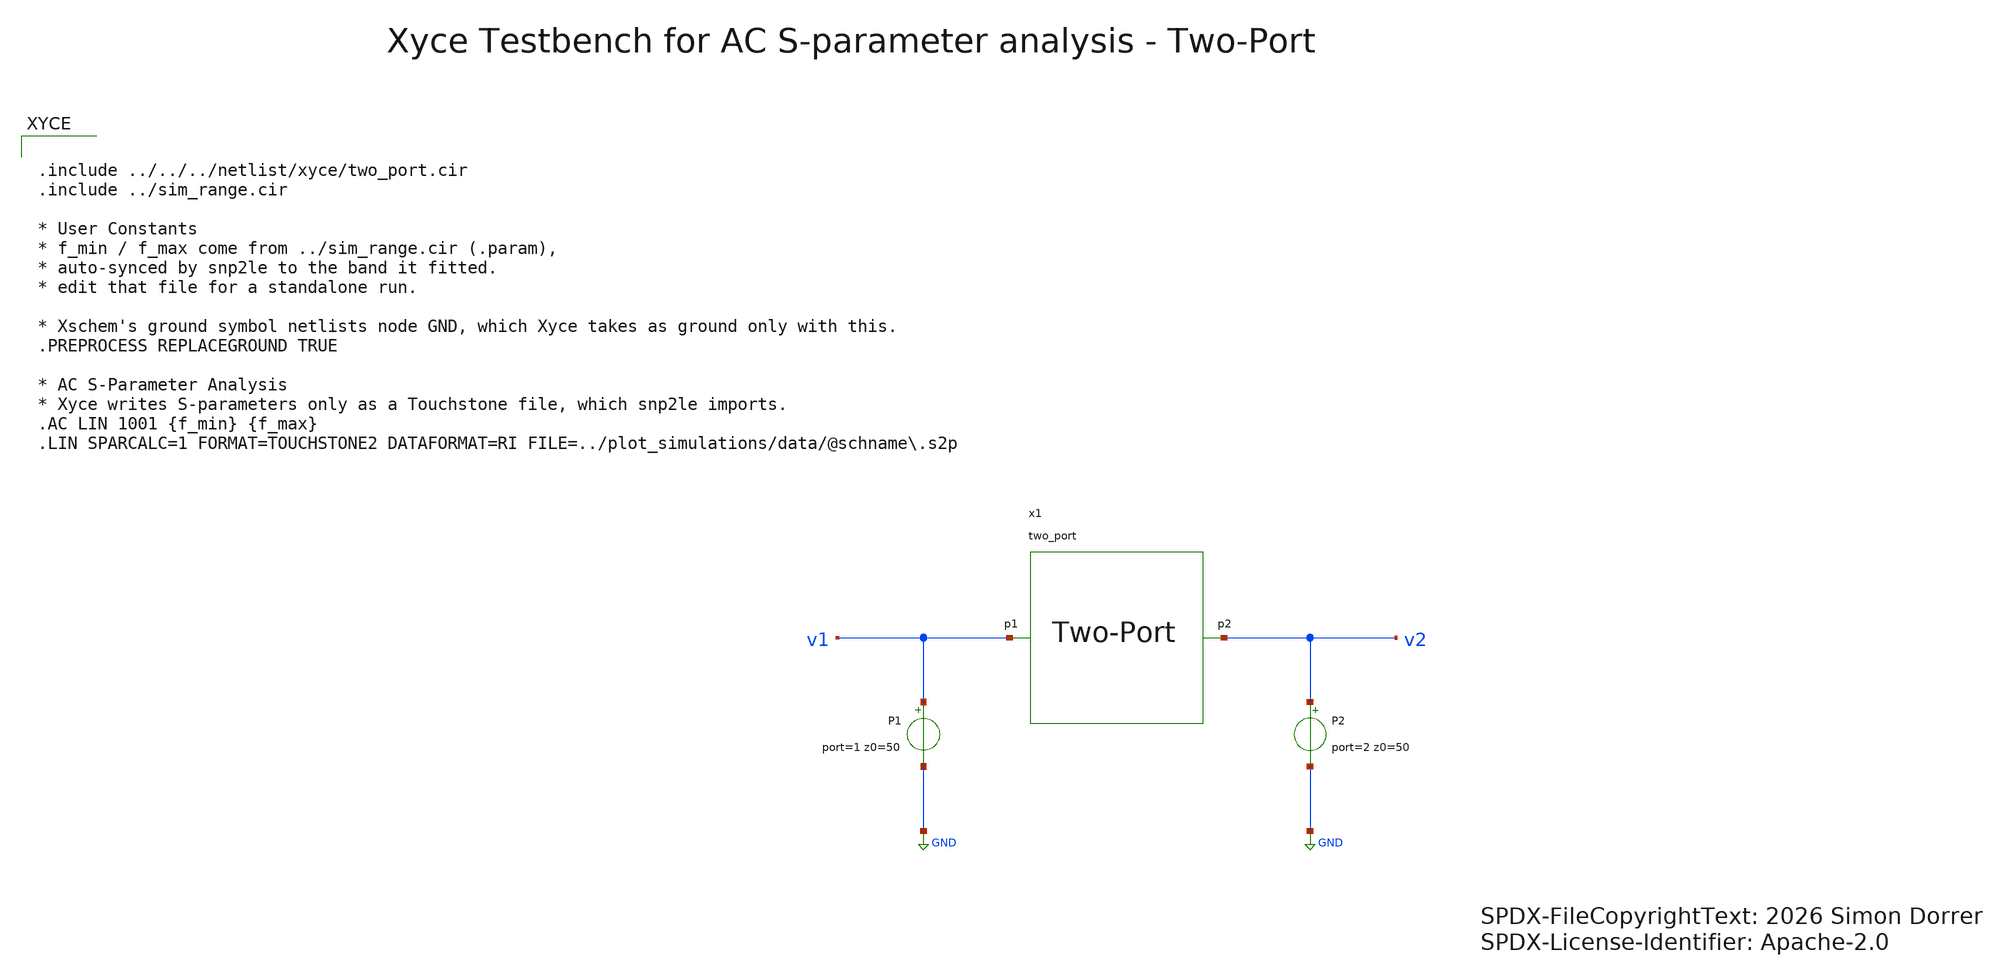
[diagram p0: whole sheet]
** sch_path: testbenches/xschem/two_port_tb_acsp_xyce.sch
* SPDX-FileCopyrightText: 2026 Simon Dorrer
* SPDX-License-Identifier: Apache-2.0
**.subckt two_port_tb_acsp_xyce
P1 v1 GND port=1 z0=50
P2 v2 GND port=2 z0=50
x1 v1 v2 two_port
**** begin user architecture code


.include ../../../netlist/xyce/two_port.cir
.include ../sim_range.cir

* User Constants
* f_min / f_max come from ../sim_range.cir (.param),
* auto-synced by snp2le to the band it fitted.
* edit that file for a standalone run.

* Xschem's ground symbol netlists node GND, which Xyce takes as ground only with this.
.PREPROCESS REPLACEGROUND TRUE

* AC S-Parameter Analysis
* Xyce writes S-parameters only as a Touchstone file, which snp2le imports.
.AC LIN 1001 {f_min} {f_max}
.LIN SPARCALC=1 FORMAT=TOUCHSTONE2 DATAFORMAT=RI FILE=../plot_simulations/data/@schname\.s2p


**** end user architecture code
**.ends
.GLOBAL GND
.end
